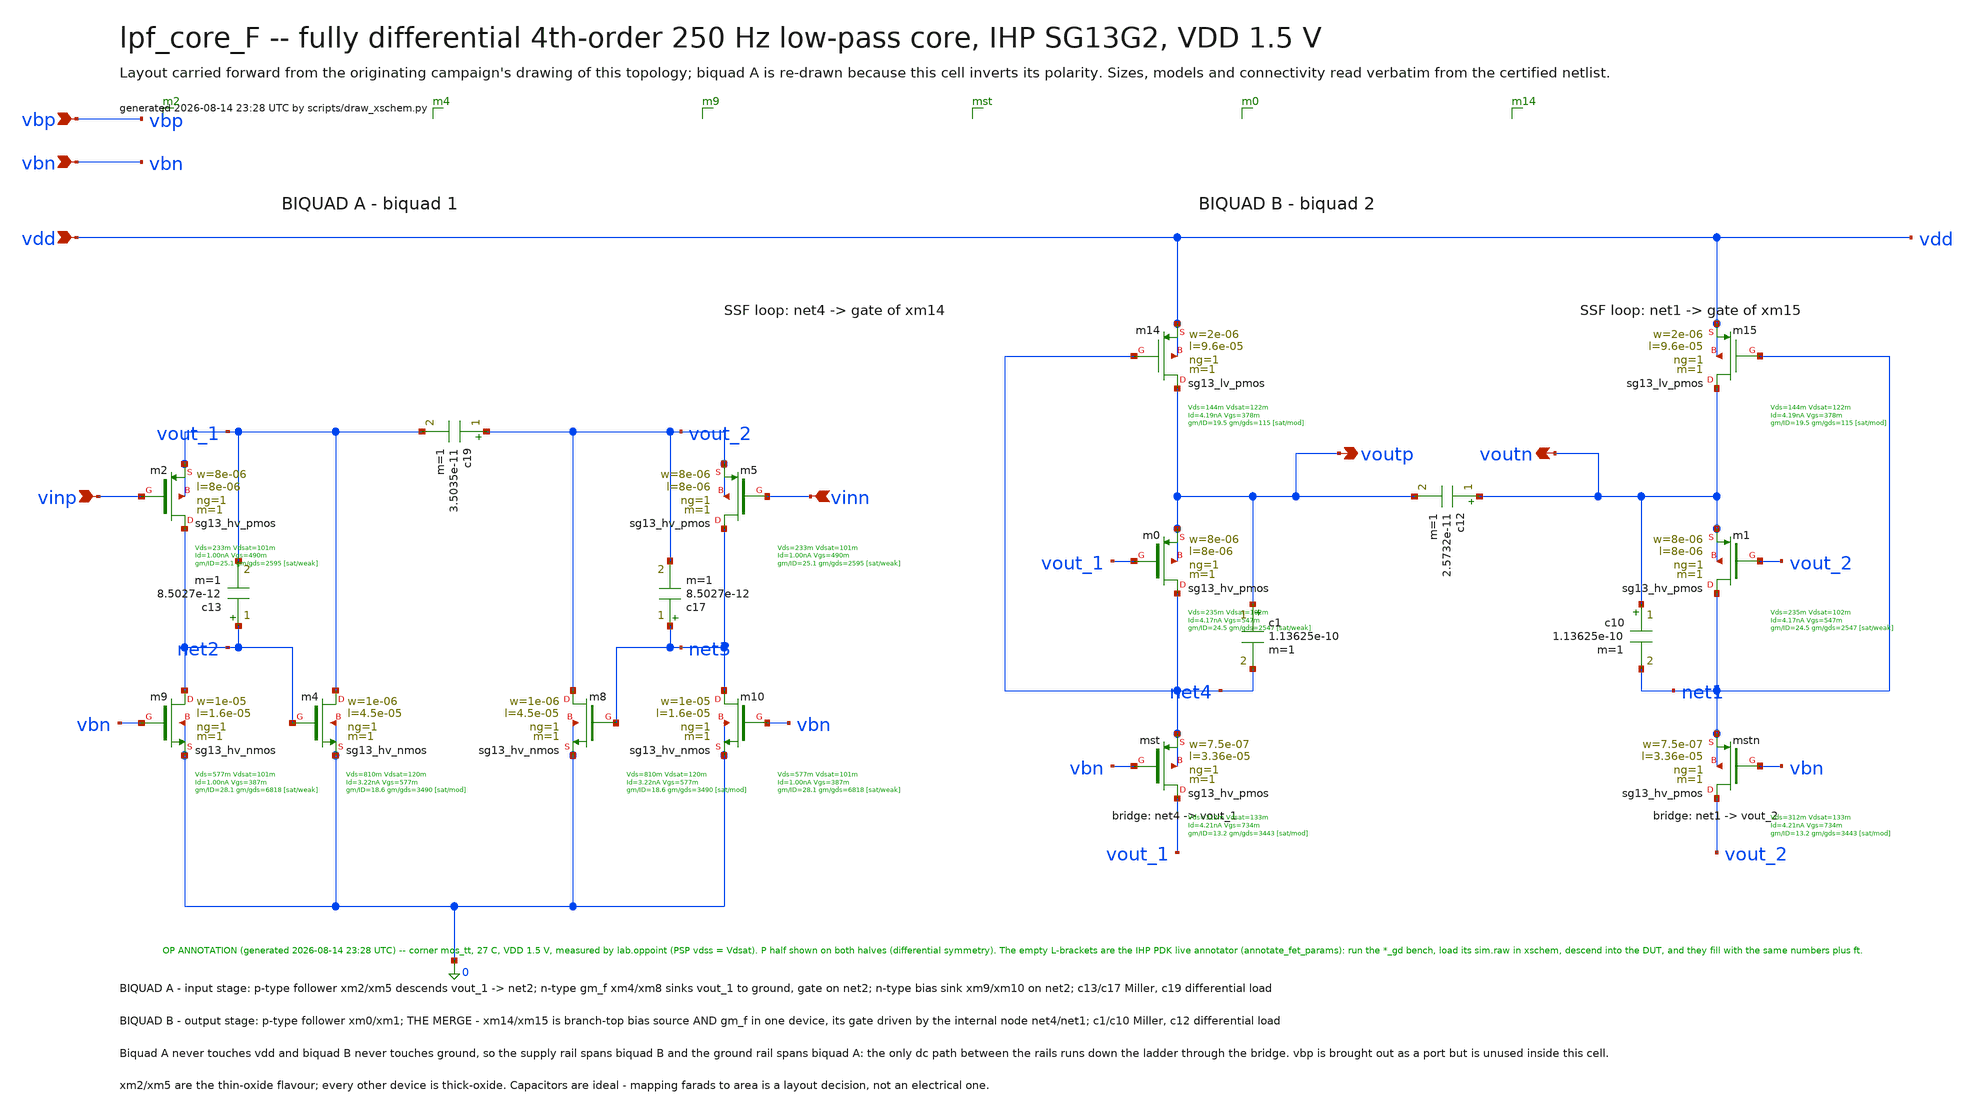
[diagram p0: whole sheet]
** sch_path: signoff/F-minnoise/lpf_core_F.sch
**.subckt lpf_core_F vinp vinn voutp voutn vdd vbn vbp
*.ipin vinp
*.ipin vinn
*.opin voutp
*.opin voutn
*.ipin vdd
*.ipin vbn
*.ipin vbp
Xm2 net2 vinp vout_1 vout_1 sg13_hv_pmos w=8e-06 l=8e-06 ng=1 m=1 mm_ok=1
Xm5 net3 vinn vout_2 vout_2 sg13_hv_pmos w=8e-06 l=8e-06 ng=1 m=1 mm_ok=1
Xm4 vout_1 net2 0 0 sg13_hv_nmos w=1e-06 l=4.5e-05 ng=1 m=1 mm_ok=1
Xm8 vout_2 net3 0 0 sg13_hv_nmos w=1e-06 l=4.5e-05 ng=1 m=1 mm_ok=1
Xm9 net2 vbn 0 0 sg13_hv_nmos w=1e-05 l=1.6e-05 ng=1 m=1 mm_ok=1
Xm10 net3 vbn 0 0 sg13_hv_nmos w=1e-05 l=1.6e-05 ng=1 m=1 mm_ok=1
Xmst vout_1 vbn net4 net4 sg13_hv_pmos w=7.5e-07 l=3.36e-05 ng=1 m=1 mm_ok=1
Xmstn vout_2 vbn net1 net1 sg13_hv_pmos w=7.5e-07 l=3.36e-05 ng=1 m=1 mm_ok=1
Xm0 net4 vout_1 voutp voutp sg13_hv_pmos w=8e-06 l=8e-06 ng=1 m=1 mm_ok=1
Xm1 net1 vout_2 voutn voutn sg13_hv_pmos w=8e-06 l=8e-06 ng=1 m=1 mm_ok=1
Xm14 voutp net4 vdd vdd sg13_lv_pmos w=2e-06 l=9.6e-05 ng=1 m=1 mm_ok=1
Xm15 voutn net1 vdd vdd sg13_lv_pmos w=2e-06 l=9.6e-05 ng=1 m=1 mm_ok=1
c13 net2 vout_1 8.5027e-12 m=1
c17 net3 vout_2 8.5027e-12 m=1
c19 vout_2 vout_1 3.5035e-11 m=1
c1 voutp net4 1.13625e-10 m=1
c10 voutn net1 1.13625e-10 m=1
c12 voutn voutp 2.5732e-11 m=1
**.ends
.end
